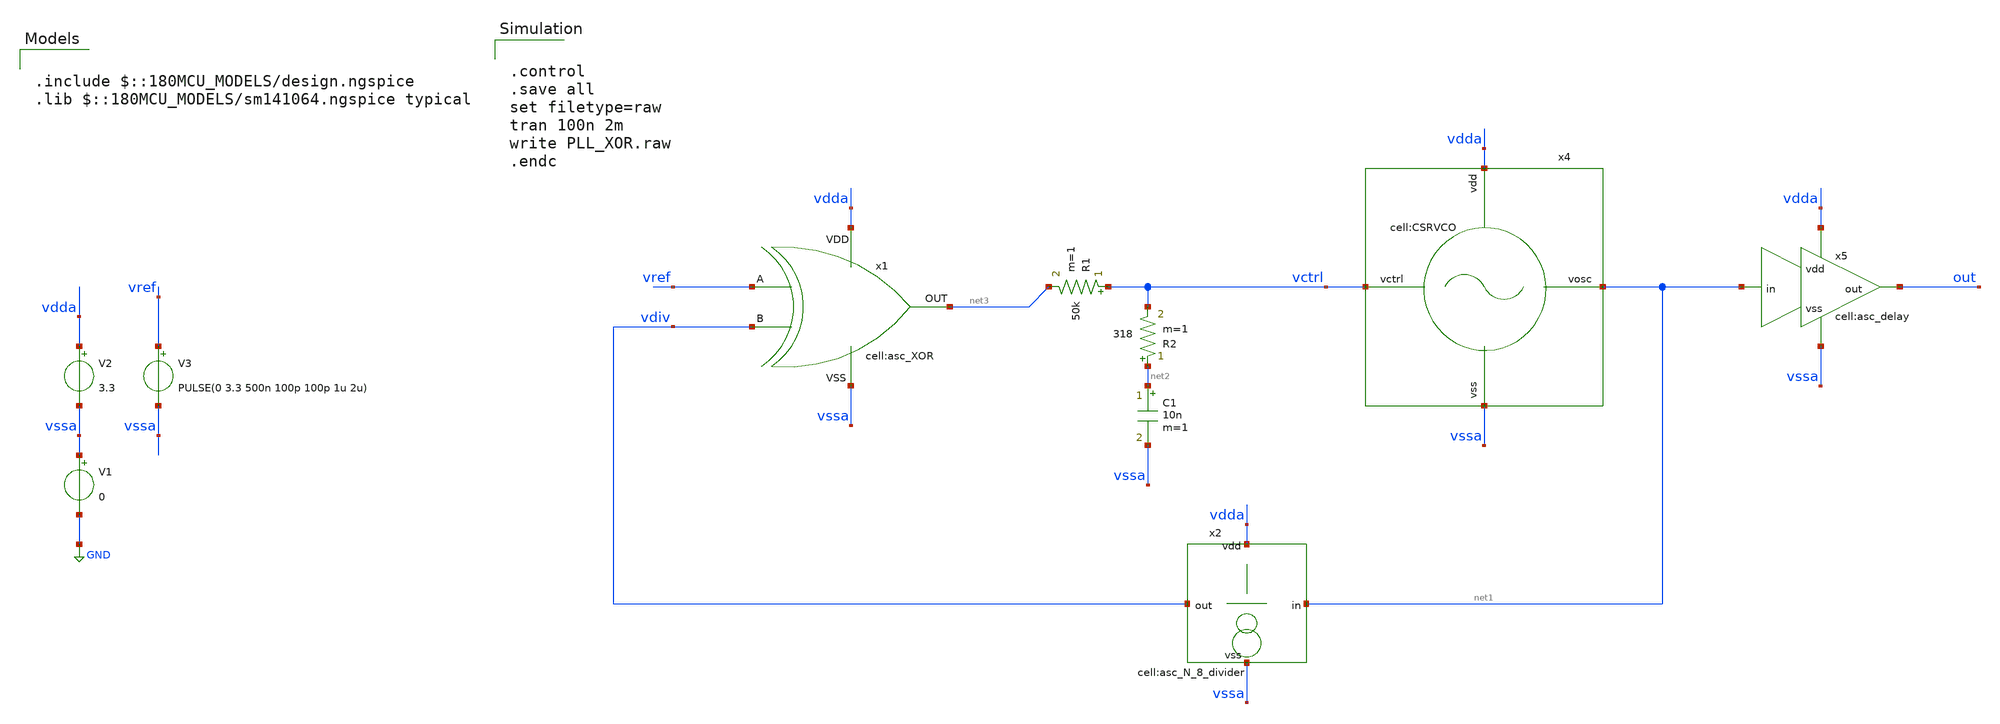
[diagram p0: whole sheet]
** sch_path: designs/libs/tb_analog/tb_xor_pll/tb_xor_pll.sch
**.subckt tb_xor_pll
V1 vssa GND 0
V2 vdda vssa 3.3
V3 vref vssa PULSE(0 3.3 500n 100p 100p 1u 2u)
x4 vctrl vdda vssa net1 CSRVCO
x5 net1 vssa out vdda asc_delay
C1 net2 vssa 10n m=1
R1 vctrl net3 50k m=1
x1 vdda vssa net3 vref vdiv asc_XOR
x2 net1 vdiv vdda vssa asc_N_8_divider
R2 net2 vctrl 318 m=1
**** begin user architecture code

.include $::180MCU_MODELS/design.ngspice
.lib $::180MCU_MODELS/sm141064.ngspice typical



.control
.save all
set filetype=raw
tran 100n 2m
write PLL_XOR.raw
.endc


**** end user architecture code
**.ends
.GLOBAL GND
.end
